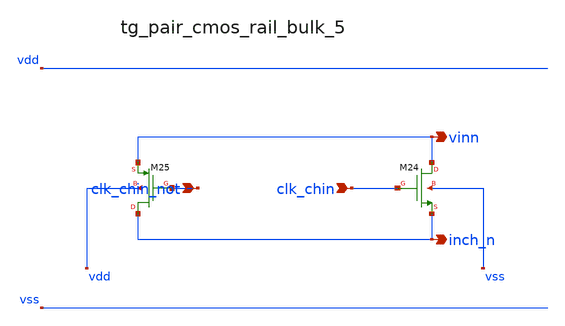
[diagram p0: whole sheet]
** sch_path: analog-db/raw/ia_002_fan_chopper_simple/hier/blocks/tg_pair_cmos_rail_bulk_5.sch
**.subckt tg_pair_cmos_rail_bulk_5 clk_chin_not clk_chin vinn inch_n
*.ipin clk_chin_not
*.ipin clk_chin
*.opin vinn
*.opin inch_n
XM24 vinn clk_chin inch_n vss sg13_lv_nmos w=x_dut_xm24_w l=x_dut_xm24_l ng=1 m=x_dut_xm24_m
XM25 inch_n clk_chin_not vinn vdd sg13_lv_pmos w=x_dut_xm25_w l=x_dut_xm25_l ng=1 m=x_dut_xm25_m
**.ends
.end
